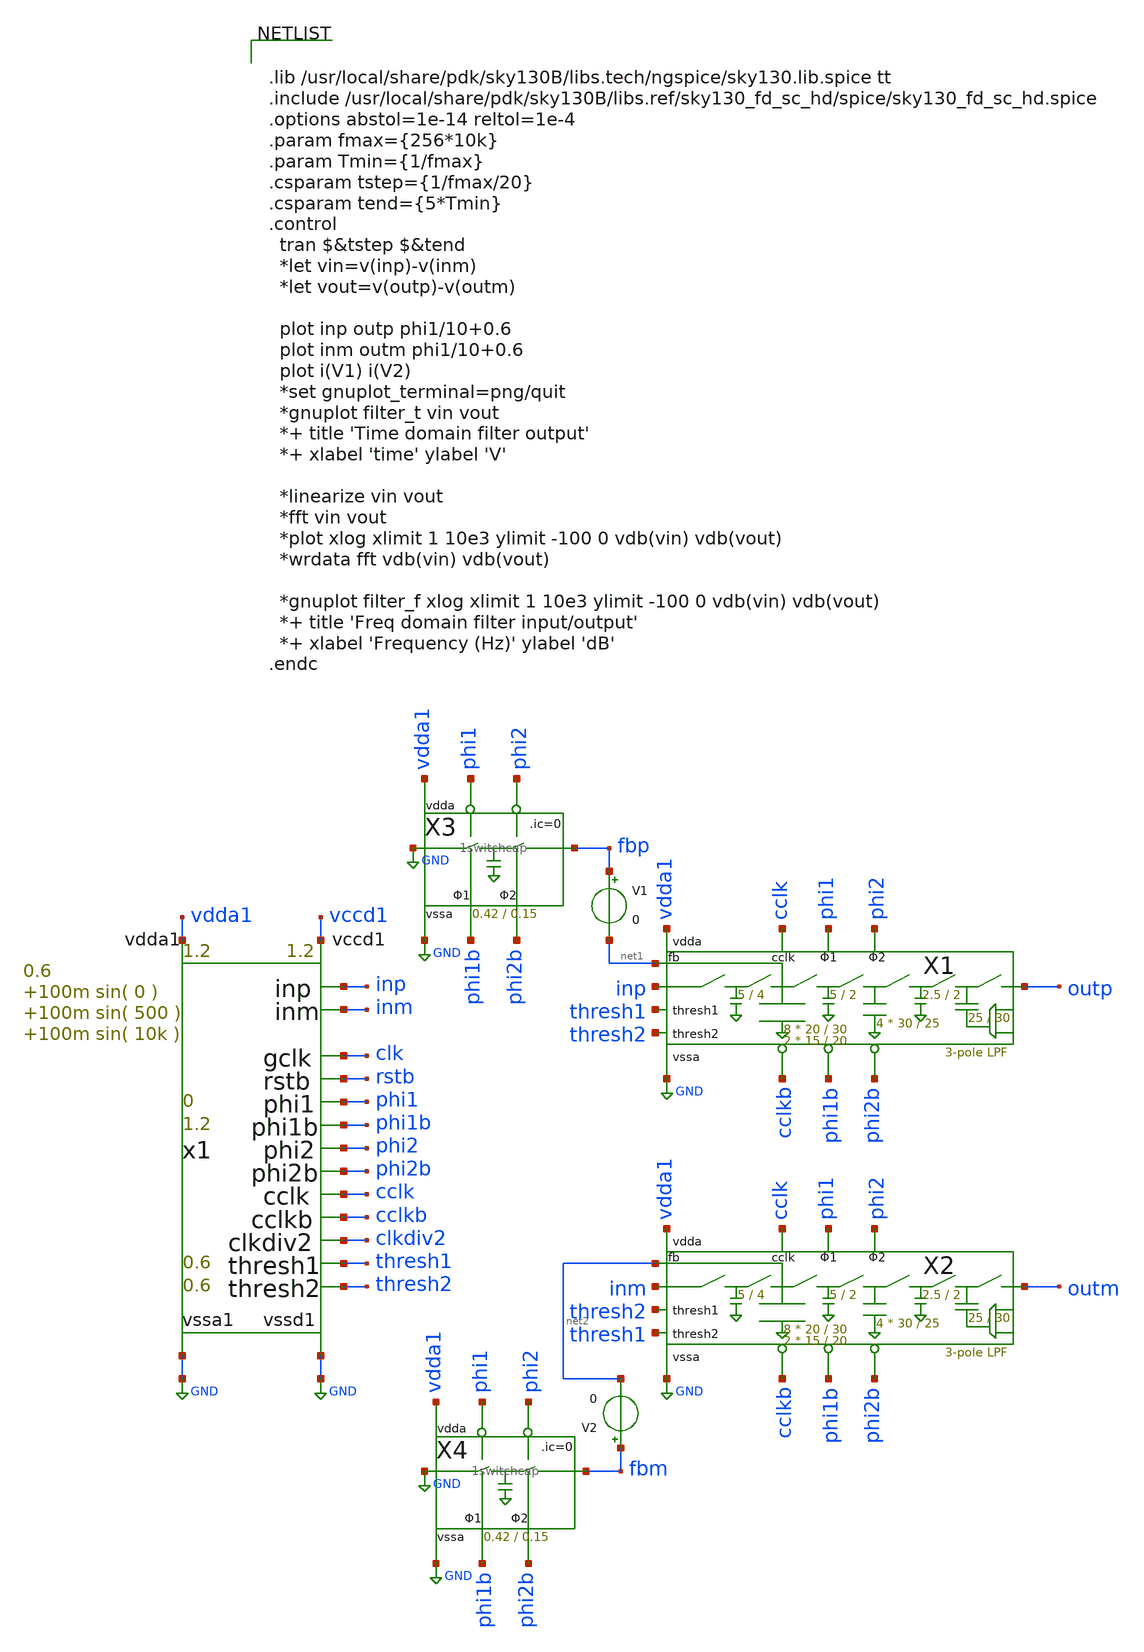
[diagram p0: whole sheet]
** sch_path: xschem/Switched_Caps/filter_fb_tb.sch
**.subckt filter_fb_tb
x1 thresh1 thresh2 vdda1 GND inp inm clk rstb vccd1 GND phi1 phi1b phi2 phi2b cclk cclkb clkdiv2 risc_signals
+ p_vdda1=1.2 p_vccd1=1.2 p_fclk={256*10k} p_duty_cycle=0.5 p_rstb_delay={1.5/p_fclk} p_rstb_tr=5n p_thresh1=0.6
+ p_thresh2=0.6 p_vpb=0 p_vnb=1.2 p_vcm=0.6 p_amp1=100m p_f1=0 p_amp2=100m p_f2=500 p_amp3=100m p_f3=10k
X1 inp outp phi2 phi1 phi1b phi2b cclk cclkb thresh1 thresh2 vdda1 GND net1 filter WC1=20 LC1=30
+ WC1B=15 LC1B=20 WC2=30 LC2=25 WC3=25 LC3=30 WCS1=5 LCS1=4 WCS2=5 LCS2=2 WCS3=2.5 LCS3=2
X2 inm outm phi2 phi1 phi1b phi2b cclk cclkb thresh2 thresh1 vdda1 GND net2 filter WC1=20 LC1=30
+ WC1B=15 LC1B=20 WC2=30 LC2=25 WC3=25 LC3=30 WCS1=5 LCS1=4 WCS2=5 LCS2=2 WCS3=2.5 LCS3=2
X3 GND fbp phi2b phi1b phi1 phi2 vdda1 GND 1switchcap Wcap1=0.42 Lcap1=0.15
X4 GND fbm phi2b phi1b phi1 phi2 vdda1 GND 1switchcap Wcap1=0.42 Lcap1=0.15
V1 fbp net1 0
V2 fbm net2 0
**** begin user architecture code


.lib /usr/local/share/pdk/sky130B/libs.tech/ngspice/sky130.lib.spice tt
.include /usr/local/share/pdk/sky130B/libs.ref/sky130_fd_sc_hd/spice/sky130_fd_sc_hd.spice
.options abstol=1e-14 reltol=1e-4
.param fmax={256*10k}
.param Tmin={1/fmax}
.csparam tstep={1/fmax/20}
.csparam tend={5*Tmin}
.control
  tran $&tstep $&tend
  *let vin=v(inp)-v(inm)
  *let vout=v(outp)-v(outm)

  plot inp outp phi1/10+0.6
  plot inm outm phi1/10+0.6
  plot i(V1) i(V2)
  *set gnuplot_terminal=png/quit
  *gnuplot filter_t vin vout
  *+ title 'Time domain filter output'
  *+ xlabel 'time' ylabel 'V'

  *linearize vin vout
  *fft vin vout
  *plot xlog xlimit 1 10e3 ylimit -100 0 vdb(vin) vdb(vout)
  *wrdata fft vdb(vin) vdb(vout)

  *gnuplot filter_f xlog xlimit 1 10e3 ylimit -100 0 vdb(vin) vdb(vout)
  *+ title 'Freq domain filter input/output'
  *+ xlabel 'Frequency (Hz)' ylabel 'dB'
.endc


**** end user architecture code
**.ends

* expanding   symbol:  risc_signals.sym # of pins=17
** sym_path: xschem/risc_signals.sym
** sch_path: xschem/risc_signals.sch
.subckt risc_signals thresh1 thresh2 vdda1 vssa1 inp inm gclk rstb vccd1 vssd1 phi1 phi1b phi2 phi2b
+ cclk cclkb clkdiv2   p_vdda1=1.2  p_vccd1=1.2  p_fclk={256*10k}  p_duty_cycle=0.5  p_rstb_delay={1.5/p_fclk}
+  p_rstb_tr=5n  p_thresh1=0.7  p_thresh2=0.65  p_vpb=0  p_vnb=1.2  p_vcm=0.6  p_amp1=100m  p_f1={256*10k}
+  p_amp2=0  p_f2=0  p_amp3=0  p_f3=0
*.opin thresh1
*.opin thresh2
*.opin vdda1
*.opin vssa1
*.opin inp
*.opin inm
*.opin phi1
*.opin phi1b
*.opin vccd1
*.opin vssd1
*.opin gclk
*.opin rstb
*.opin phi2
*.opin phi2b
*.opin cclk
*.opin cclkb
*.opin clkdiv2
vdda1 vdda1 vssa1 DC {p_vdda1}
vthresh1 thresh1 vssa1 DC {p_thresh1}
vthresh2 thresh2 vssa1 DC {p_thresh2}
vinp1 inp inp2 DC 0 SIN(0 {p_amp1} {p_f1})
vinm1 inm inm2 DC 0 SIN(0 {-p_amp1} {p_f1})
vpb vpb vssa1 DC {p_vpb}
vnb vnb vssa1 DC {p_vnb}
vinp2 inp2 inp3 DC 0 SIN(0 {p_amp2} {p_f2})
vinp3 inp3 vcm DC 0 SIN(0 {p_amp3} {p_f3})
vinm2 inm2 inm3 DC 0 SIN(0 {-p_amp2} {p_f2})
vinm3 inm3 vcm DC 0 SIN(0 {-p_amp3} {p_f3})
vcm vcm vssa1 DC {p_vcm}
vdda2 vccd1 vssd1 DC {p_vccd1}
Vclk clk vssd1 DC 0 PULSE (0 p_vccd1 1n 1n 1n {p_duty_cycle*1/p_fclk} {1/p_fclk} 0
Vrstb rstb vssd1 DC 0 PWL ( 0 0 p_rstb_delay 0 {p_rstb_delay + p_rstb_tr} p_vccd1)
x1 clk rstb vssd1 vssd1 vccd1 vccd1 gclk sky130_fd_sc_hd__dlclkp_1
x2 rstb gclk phi2b phi2 phi1b phi1 cclkb cclk clkdiv2 vpb vnb vdda1 vssa1 vccd1 vssd1 filter_clkgen
.ends


* expanding   symbol:  Switched_Caps/filter.sym # of pins=13
** sym_path: xschem/Switched_Caps/filter.sym
** sch_path: xschem/Switched_Caps/filter.sch
.subckt filter in out phi2 phi1 phi1b phi2b cclk cclkb thresh1 thresh2 vdda vssa fb  WC1=20 LC1=30
+ WC1B=15 LC1B=20 WC2=30 LC2=25 WC3=25 LC3=30 WCS1=5 LCS1=4 WCS2=5 LCS2=2 WCS3=2.5 LCS3=2
*.ipin in
*.opin out
*.ipin phi1
*.ipin phi2
*.ipin phi1b
*.ipin phi2b
*.ipin cclk
*.ipin cclkb
*.ipin thresh1
*.ipin thresh2
*.ipin vdda
*.ipin vssa
*.ipin fb
XC12 vssa fb sky130_fd_pr__cap_mim_m3_2 W=WC1 L=LC1 MF=1 m=1
XCS1 net1 vssa sky130_fd_pr__cap_mim_m3_1 W=WCS1 L=LCS1 MF=1 m=1
XC11 fb vssa sky130_fd_pr__cap_mim_m3_1 W=WC1 L=LC1 MF=1 m=1
XCS2 net2 vssa sky130_fd_pr__cap_mim_m3_1 W=WCS2 L=LCS2 MF=1 m=1
XC3 net4 out sky130_fd_pr__cap_mim_m3_2 W=WC3 L=LC3 MF=1 m=1
XCS3 net3 vssa sky130_fd_pr__cap_mim_m3_1 W=WCS3 L=LCS3 MF=1 m=1
XC14 vssa fb sky130_fd_pr__cap_mim_m3_2 W=WC1 L=LC1 MF=1 m=1
XC13 fb vssa sky130_fd_pr__cap_mim_m3_1 W=WC1 L=LC1 MF=1 m=1
XC16 vssa fb sky130_fd_pr__cap_mim_m3_2 W=WC1 L=LC1 MF=1 m=1
XC15 fb vssa sky130_fd_pr__cap_mim_m3_1 W=WC1 L=LC1 MF=1 m=1
XC18 vssa fb sky130_fd_pr__cap_mim_m3_2 W=WC1 L=LC1 MF=1 m=1
XC17 fb vssa sky130_fd_pr__cap_mim_m3_1 W=WC1 L=LC1 MF=1 m=1
XC22 vssa stage2 sky130_fd_pr__cap_mim_m3_2 W=WC2 L=LC2 MF=1 m=1
XC21 stage2 vssa sky130_fd_pr__cap_mim_m3_1 W=WC2 L=LC2 MF=1 m=1
XC24 vssa stage2 sky130_fd_pr__cap_mim_m3_2 W=WC2 L=LC2 MF=1 m=1
XC23 stage2 vssa sky130_fd_pr__cap_mim_m3_1 W=WC2 L=LC2 MF=1 m=1
XC1 out net4 sky130_fd_pr__cap_mim_m3_1 W=WC3 L=LC3 MF=1 m=1
x7 thresh2 thresh1 cclk cclkb net4 vssa vdda analogMux
X1 in net1 phi1b phi1 vdda vssa transmission_gate Wpmos=0.42 Lpmos=0.18 Wnmos=0.42 Lnmos=0.18
X2 net1 fb phi2b phi2 vdda vssa transmission_gate Wpmos=0.42 Lpmos=0.18 Wnmos=0.42 Lnmos=0.18
X3 fb net2 phi1b phi1 vdda vssa transmission_gate Wpmos=0.42 Lpmos=0.18 Wnmos=0.42 Lnmos=0.18
X4 net2 stage2 phi2b phi2 vdda vssa transmission_gate Wpmos=0.42 Lpmos=0.18 Wnmos=0.42 Lnmos=0.18
X5 stage2 net3 phi1b phi1 vdda vssa transmission_gate Wpmos=0.42 Lpmos=0.18 Wnmos=0.42 Lnmos=0.18
X6 net3 out phi2b phi2 vdda vssa transmission_gate Wpmos=0.42 Lpmos=0.18 Wnmos=0.42 Lnmos=0.18
.ends


* expanding   symbol:  Switched_Caps/1switchcap.sym # of pins=8
** sym_path: xschem/Switched_Caps/1switchcap.sym
** sch_path: xschem/Switched_Caps/1switchcap.sch
.subckt 1switchcap in out phi2_clk_n phi1_clk_n phi1_clk_p phi2_clk_p vdda vssa  Wcap1=0.42
+ Lcap1=0.15
*.iopin out
*.iopin in
*.ipin phi1_clk_n
*.ipin phi1_clk_p
*.ipin phi2_clk_p
*.ipin phi2_clk_n
*.ipin vdda
*.ipin vssa
XC1 c1 GND sky130_fd_pr__cap_mim_m3_1 W=Wcap1 L=Lcap1 MF=1 m=1
**** begin user architecture code

.ic v(c1)=0 v(out)=0

**** end user architecture code
X1 in c1 phi1_clk_p phi1_clk_n vdda vssa transmission_gate Wpmos=0.42 Lpmos=0.18 Wnmos=0.42
+ Lnmos=0.18
X2 c1 out phi2_clk_p phi2_clk_n vdda vssa transmission_gate Wpmos=0.42 Lpmos=0.18 Wnmos=0.42
+ Lnmos=0.18
.ends


* expanding   symbol:  clkgen/filter_clkgen.sym # of pins=15
** sym_path: xschem/clkgen/filter_clkgen.sym
** sch_path: xschem/clkgen/filter_clkgen.sch
.subckt filter_clkgen rstb clk phi2b phi2 phi1b phi1 cclkb cclk clkdiv2 vpb vnb vdda vssa vccd vssd
*.ipin clk
*.ipin rstb
*.opin phi2
*.opin phi2b
*.opin phi1
*.opin phi1b
*.opin cclk
*.opin cclkb
*.opin clkdiv2
*.ipin vpb
*.ipin vnb
*.ipin vdda
*.ipin vssa
*.ipin vccd
*.ipin vssd
x11 clk net3 rstb vssd vssd vccd vccd clkdiv2 net3 sky130_fd_sc_hd__dfrbp_1
X4 phi2dd phi2 phi2b vdda vssa comp_clks Wpmos=1.26 Lpmos=0.18 Wnmos=0.42 Lnmos=0.18
X7 phi1dd phi1 phi1b vdda vssa comp_clks Wpmos=1.26 Lpmos=0.18 Wnmos=0.42 Lnmos=0.18
X10 div2dd cclk cclkb vdda vssa comp_clks Wpmos=1.26 Lpmos=0.18 Wnmos=0.42 Lnmos=0.18
X1 clk net1 net2 vdda vssa comp_clks_1stage Wpmos=1.26 Lpmos=0.18 Wnmos=0.42 Lnmos=0.18
x2 net4 clkdiv2 vssd vssd vccd vccd net5 sky130_fd_sc_hd__and2_0
X2 net1 phi2d vnb vdda vssa inv_weak_pulldown Wpmos=1.26 Lpmos= Wnmos= Lnmos=0.54
X5 net2 phi1d vnb vdda vssa inv_weak_pulldown Wpmos=1.26 Lpmos= Wnmos= Lnmos=0.54
X8 net5 div2d vnb vdda vssa inv_weak_pulldown Wpmos=1.26 Lpmos= Wnmos= Lnmos=0.54
X9 div2d div2dd vnb vdda vssa inv_weak_pulldown Wpmos=1.26 Lpmos= Wnmos= Lnmos=0.54
X3 phi2d phi2dd vpb vdda vssa inv_weak_pullup Wpmos=1.26 Lpmos=0.54 Wnmos= Lnmos=
X6 phi1d phi1dd vpb vdda vssa inv_weak_pullup Wpmos=1.26 Lpmos=0.54 Wnmos= Lnmos=
x1 clk vssd vssd vccd vccd net6 sky130_fd_sc_hd__buf_1
x3 net6 vssd vssd vccd vccd net7 sky130_fd_sc_hd__buf_1
x4 net7 vssd vssd vccd vccd net4 sky130_fd_sc_hd__buf_1
.ends


* expanding   symbol:  mux/analogMux.sym # of pins=7
** sym_path: xschem/mux/analogMux.sym
** sch_path: xschem/mux/analogMux.sch
.subckt analogMux vref2 vref1 c cbar out vssa vdda
*.ipin vref1
*.opin out
*.ipin vref2
*.ipin c
*.ipin cbar
*.ipin vssa
*.ipin vdda
XM2 vref1 c out vssa sky130_fd_pr__nfet_01v8 L=0.15 W=0.42 nf=1 ad='int((nf+1)/2) * W/nf * 0.29' as='int((nf+2)/2) * W/nf * 0.29'
+ pd='2*int((nf+1)/2) * (W/nf + 0.29)' ps='2*int((nf+2)/2) * (W/nf + 0.29)' nrd='0.29 / W' nrs='0.29 / W'
+ sa=0 sb=0 sd=0 mult=1 m=1
XM4 vref1 cbar out vdda sky130_fd_pr__pfet_01v8 L=0.15 W=0.42 nf=1 ad='int((nf+1)/2) * W/nf * 0.29' as='int((nf+2)/2) * W/nf * 0.29'
+ pd='2*int((nf+1)/2) * (W/nf + 0.29)' ps='2*int((nf+2)/2) * (W/nf + 0.29)' nrd='0.29 / W' nrs='0.29 / W'
+ sa=0 sb=0 sd=0 mult=1 m=1
XM7 out cbar vref2 vssa sky130_fd_pr__nfet_01v8 L=0.15 W=0.42 nf=1 ad='int((nf+1)/2) * W/nf * 0.29' as='int((nf+2)/2) * W/nf * 0.29'
+ pd='2*int((nf+1)/2) * (W/nf + 0.29)' ps='2*int((nf+2)/2) * (W/nf + 0.29)' nrd='0.29 / W' nrs='0.29 / W'
+ sa=0 sb=0 sd=0 mult=1 m=1
XM8 out c vref2 vdda sky130_fd_pr__pfet_01v8 L=0.15 W=0.42 nf=1 ad='int((nf+1)/2) * W/nf * 0.29' as='int((nf+2)/2) * W/nf * 0.29'
+ pd='2*int((nf+1)/2) * (W/nf + 0.29)' ps='2*int((nf+2)/2) * (W/nf + 0.29)' nrd='0.29 / W' nrs='0.29 / W'
+ sa=0 sb=0 sd=0 mult=1 m=1
.ends


* expanding   symbol:  transmission_gate/transmission_gate.sym # of pins=6
** sym_path: xschem/transmission_gate/transmission_gate.sym
** sch_path: xschem/transmission_gate/transmission_gate.sch
.subckt transmission_gate in out ctrl_ ctrl vdda vssa  Wpmos=Wpmos Lpmos=Lpmos Wnmos=Wnmos
+ Lnmos=Lnmos
*.iopin in
*.iopin out
*.ipin ctrl_
*.ipin ctrl
*.ipin vdda
*.ipin vssa
XM1 out ctrl in vssa sky130_fd_pr__nfet_01v8 L=Lnmos W=Wnmos nf=1 ad='int((nf+1)/2) * W/nf * 0.29' as='int((nf+2)/2) * W/nf * 0.29'
+ pd='2*int((nf+1)/2) * (W/nf + 0.29)' ps='2*int((nf+2)/2) * (W/nf + 0.29)' nrd='0.29 / W' nrs='0.29 / W'
+ sa=0 sb=0 sd=0 mult=1 m=1
XM2 out ctrl_ in vdda sky130_fd_pr__pfet_01v8 L=Lpmos W=1.26 nf=1 ad='int((nf+1)/2) * W/nf * 0.29' as='int((nf+2)/2) * W/nf * 0.29'
+ pd='2*int((nf+1)/2) * (W/nf + 0.29)' ps='2*int((nf+2)/2) * (W/nf + 0.29)' nrd='0.29 / W' nrs='0.29 / W'
+ sa=0 sb=0 sd=0 mult=1 m=1
.ends


* expanding   symbol:  clkgen/comp_clks.sym # of pins=5
** sym_path: xschem/clkgen/comp_clks.sym
** sch_path: xschem/clkgen/comp_clks.sch
.subckt comp_clks clk clka clkb vdd vss  Wpmos=Wpmos Lpmos=Lpmos Wnmos=Wnmos Lnmos=Lnmos
*.ipin clk
*.opin clka
*.opin clkb
*.iopin vdd
*.iopin vss
X1 clk clki vdd vss inv Wpmos=Wpmos Lpmos=Lpmos Wnmos=Wnmos Lnmos=Lnmos
X2 clki clka vdd vss inv Wpmos=Wpmos Lpmos=Lpmos Wnmos=Wnmos Lnmos=Lnmos
X4 clkt clkb vdd vss inv Wpmos=Wpmos Lpmos=Lpmos Wnmos=Wnmos Lnmos=Lnmos
x3 clk clkt vss vdd vdd vss tg Wpmos=Wpmos Lpmos=Lpmos Wnmos=Wnmos Lnmos=Lnmos
.ends


* expanding   symbol:  clkgen/comp_clks_1stage.sym # of pins=5
** sym_path: xschem/clkgen/comp_clks_1stage.sym
** sch_path: xschem/clkgen/comp_clks_1stage.sch
.subckt comp_clks_1stage clk clka clkb vdda vssa  Wpmos=1.26 Lpmos=0.18 Wnmos=0.42 Lnmos=0.18
*.ipin clk
*.opin clka
*.opin clkb
*.ipin vdda
*.ipin vssa
X3 clk clkb vssa vdda vdda vssa transmission_gate Wpmos=Wpmos Lpmos=Lpmos Wnmos=Wnmos Lnmos=Lnmos
X1 clk clka vdda vssa inv Wpmos=Wpmos Lpmos=Lpmos Wnmos=Wnmos Lnmos=Lnmos
.ends


* expanding   symbol:  inv/inv_weak_pulldown.sym # of pins=5
** sym_path: xschem/inv/inv_weak_pulldown.sym
** sch_path: xschem/inv/inv_weak_pulldown.sch
.subckt inv_weak_pulldown in out Vnb vdda vssa  Wpmos=1.26 Lmin=0.18 Wmin=0.42 Lnmos=0.54
*.ipin in
*.iopin out
*.ipin Vnb
*.ipin vdda
*.ipin vssa
XM1 net1 in vssa vssa sky130_fd_pr__nfet_01v8 L=Lmin W=Wmin nf=1 ad='int((nf+1)/2) * W/nf * 0.29' as='int((nf+2)/2) * W/nf * 0.29'
+ pd='2*int((nf+1)/2) * (W/nf + 0.29)' ps='2*int((nf+2)/2) * (W/nf + 0.29)' nrd='0.29 / W' nrs='0.29 / W'
+ sa=0 sb=0 sd=0 mult=1 m=1
XM3 out Vnb net1 vssa sky130_fd_pr__nfet_01v8 L=Lnmos W=Wmin nf=1 ad='int((nf+1)/2) * W/nf * 0.29' as='int((nf+2)/2) * W/nf * 0.29'
+ pd='2*int((nf+1)/2) * (W/nf + 0.29)' ps='2*int((nf+2)/2) * (W/nf + 0.29)' nrd='0.29 / W' nrs='0.29 / W'
+ sa=0 sb=0 sd=0 mult=1 m=1
XM4 out in vdda vdda sky130_fd_pr__pfet_01v8 L=Lmin W=Wpmos nf=1 ad='int((nf+1)/2) * W/nf * 0.29' as='int((nf+2)/2) * W/nf * 0.29'
+ pd='2*int((nf+1)/2) * (W/nf + 0.29)' ps='2*int((nf+2)/2) * (W/nf + 0.29)' nrd='0.29 / W' nrs='0.29 / W'
+ sa=0 sb=0 sd=0 mult=1 m=1
.ends


* expanding   symbol:  inv/inv_weak_pullup.sym # of pins=5
** sym_path: xschem/inv/inv_weak_pullup.sym
** sch_path: xschem/inv/inv_weak_pullup.sch
.subckt inv_weak_pullup in out Vpb vdda vssa  Wpmos=1.26 Lpmos=0.54 Wmin=0.42 Lmin=0.18
*.ipin in
*.iopin out
*.ipin Vpb
*.ipin vdda
*.ipin vssa
XM1 out in vssa vssa sky130_fd_pr__nfet_01v8 L=Lmin W=Wmin nf=1 ad='int((nf+1)/2) * W/nf * 0.29' as='int((nf+2)/2) * W/nf * 0.29'
+ pd='2*int((nf+1)/2) * (W/nf + 0.29)' ps='2*int((nf+2)/2) * (W/nf + 0.29)' nrd='0.29 / W' nrs='0.29 / W'
+ sa=0 sb=0 sd=0 mult=1 m=1
XM3 out Vpb net1 vdda sky130_fd_pr__pfet_01v8 L=Lmin W=Wpmos nf=1 ad='int((nf+1)/2) * W/nf * 0.29' as='int((nf+2)/2) * W/nf * 0.29'
+ pd='2*int((nf+1)/2) * (W/nf + 0.29)' ps='2*int((nf+2)/2) * (W/nf + 0.29)' nrd='0.29 / W' nrs='0.29 / W'
+ sa=0 sb=0 sd=0 mult=1 m=1
XM5 net1 in vdda vdda sky130_fd_pr__pfet_01v8 L=Lmin W=Wpmos nf=1 ad='int((nf+1)/2) * W/nf * 0.29' as='int((nf+2)/2) * W/nf * 0.29'
+ pd='2*int((nf+1)/2) * (W/nf + 0.29)' ps='2*int((nf+2)/2) * (W/nf + 0.29)' nrd='0.29 / W' nrs='0.29 / W'
+ sa=0 sb=0 sd=0 mult=1 m=1
.ends


* expanding   symbol:  xschem/inv/inv.sym # of pins=4
** sym_path: xschem/inv/inv.sym
** sch_path: xschem/inv/inv.sch
.subckt inv in out vdd vss  Wpmos=Wpmos Lpmos=Lpmos Wnmos=Wnmos Lnmos=Lnmos
*.ipin in
*.iopin out
*.iopin vdd
*.iopin vss
XM1 vss in out vss sky130_fd_pr__nfet_01v8 L=Lnmos W=Wnmos nf=1 ad='int((nf+1)/2) * W/nf * 0.29' as='int((nf+2)/2) * W/nf * 0.29'
+ pd='2*int((nf+1)/2) * (W/nf + 0.29)' ps='2*int((nf+2)/2) * (W/nf + 0.29)' nrd='0.29 / W' nrs='0.29 / W'
+ sa=0 sb=0 sd=0 mult=1 m=1
XM2 vdd in out vdd sky130_fd_pr__pfet_01v8 L=Lpmos W=Wpmos nf=1 ad='int((nf+1)/2) * W/nf * 0.29' as='int((nf+2)/2) * W/nf * 0.29'
+ pd='2*int((nf+1)/2) * (W/nf + 0.29)' ps='2*int((nf+2)/2) * (W/nf + 0.29)' nrd='0.29 / W' nrs='0.29 / W'
+ sa=0 sb=0 sd=0 mult=1 m=1
.ends


* expanding   symbol:  xschem/transmission_gate/tg.sym # of pins=6
** sym_path: xschem/transmission_gate/tg.sym
** sch_path: xschem/transmission_gate/tg.sch
.subckt tg in out ctrl_ ctrl vdda vssa  Wpmos=0.42 Lpmos=0.18 Wnmos=0.42 Lnmos=0.18
*.iopin in
*.iopin out
*.ipin ctrl_
*.ipin ctrl
*.ipin vdda
*.ipin vssa
XM1 out ctrl in vssa sky130_fd_pr__nfet_01v8 L=Lnmos W=Wnmos nf=1 ad='int((nf+1)/2) * W/nf * 0.29' as='int((nf+2)/2) * W/nf * 0.29'
+ pd='2*int((nf+1)/2) * (W/nf + 0.29)' ps='2*int((nf+2)/2) * (W/nf + 0.29)' nrd='0.29 / W' nrs='0.29 / W'
+ sa=0 sb=0 sd=0 mult=1 m=1
XM2 out ctrl_ in vdda sky130_fd_pr__pfet_01v8 L=Lpmos W=Wpmos nf=1 ad='int((nf+1)/2) * W/nf * 0.29' as='int((nf+2)/2) * W/nf * 0.29'
+ pd='2*int((nf+1)/2) * (W/nf + 0.29)' ps='2*int((nf+2)/2) * (W/nf + 0.29)' nrd='0.29 / W' nrs='0.29 / W'
+ sa=0 sb=0 sd=0 mult=2 m=2
.ends

.GLOBAL GND
.end
